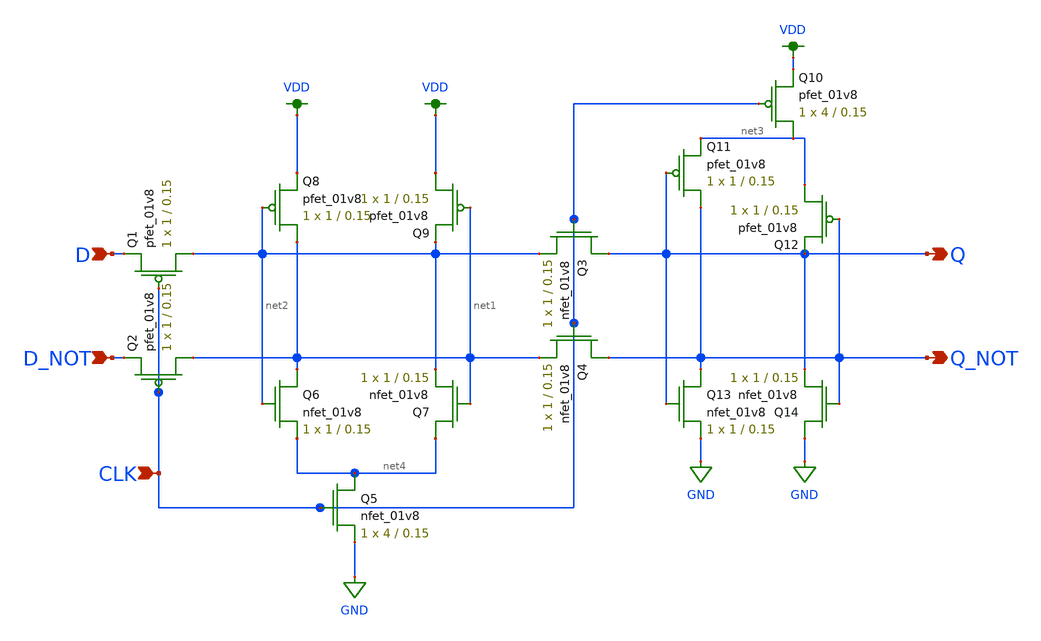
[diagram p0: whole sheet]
** sch_path: miniproject2/CSRL_Latch.sch
**.subckt CSRL_Latch D D_NOT Q Q_NOT CLK
*.ipin D
*.ipin D_NOT
*.opin Q
*.opin Q_NOT
*.ipin CLK
XQ8 net1 net2 VDD VDD sky130_fd_pr__pfet_01v8 L=0.15 W=1 nf=1 ad='int((nf+1)/2) * W/nf * 0.29' as='int((nf+2)/2) * W/nf * 0.29'
+ pd='2*int((nf+1)/2) * (W/nf + 0.29)' ps='2*int((nf+2)/2) * (W/nf + 0.29)' nrd='0.29 / W' nrs='0.29 / W'
+ sa=0 sb=0 sd=0 mult=1 m=1
XQ9 VDD net1 net2 VDD sky130_fd_pr__pfet_01v8 L=0.15 W=1 nf=1 ad='int((nf+1)/2) * W/nf * 0.29' as='int((nf+2)/2) * W/nf * 0.29'
+ pd='2*int((nf+1)/2) * (W/nf + 0.29)' ps='2*int((nf+2)/2) * (W/nf + 0.29)' nrd='0.29 / W' nrs='0.29 / W'
+ sa=0 sb=0 sd=0 mult=1 m=1
XQ1 net2 CLK D VDD sky130_fd_pr__pfet_01v8 L=0.15 W=1 nf=1 ad='int((nf+1)/2) * W/nf * 0.29' as='int((nf+2)/2) * W/nf * 0.29'
+ pd='2*int((nf+1)/2) * (W/nf + 0.29)' ps='2*int((nf+2)/2) * (W/nf + 0.29)' nrd='0.29 / W' nrs='0.29 / W'
+ sa=0 sb=0 sd=0 mult=1 m=1
XQ2 net1 CLK D_NOT VDD sky130_fd_pr__pfet_01v8 L=0.15 W=1 nf=1 ad='int((nf+1)/2) * W/nf * 0.29' as='int((nf+2)/2) * W/nf * 0.29'
+ pd='2*int((nf+1)/2) * (W/nf + 0.29)' ps='2*int((nf+2)/2) * (W/nf + 0.29)' nrd='0.29 / W' nrs='0.29 / W'
+ sa=0 sb=0 sd=0 mult=1 m=1
XQ5 net4 CLK GND GND sky130_fd_pr__nfet_01v8 L=0.15 W=4 nf=1 ad='int((nf+1)/2) * W/nf * 0.29' as='int((nf+2)/2) * W/nf * 0.29'
+ pd='2*int((nf+1)/2) * (W/nf + 0.29)' ps='2*int((nf+2)/2) * (W/nf + 0.29)' nrd='0.29 / W' nrs='0.29 / W'
+ sa=0 sb=0 sd=0 mult=1 m=1
XQ4 Q_NOT CLK net1 GND sky130_fd_pr__nfet_01v8 L=0.15 W=1 nf=1 ad='int((nf+1)/2) * W/nf * 0.29' as='int((nf+2)/2) * W/nf * 0.29'
+ pd='2*int((nf+1)/2) * (W/nf + 0.29)' ps='2*int((nf+2)/2) * (W/nf + 0.29)' nrd='0.29 / W' nrs='0.29 / W'
+ sa=0 sb=0 sd=0 mult=1 m=1
XQ3 Q CLK net2 GND sky130_fd_pr__nfet_01v8 L=0.15 W=1 nf=1 ad='int((nf+1)/2) * W/nf * 0.29' as='int((nf+2)/2) * W/nf * 0.29'
+ pd='2*int((nf+1)/2) * (W/nf + 0.29)' ps='2*int((nf+2)/2) * (W/nf + 0.29)' nrd='0.29 / W' nrs='0.29 / W'
+ sa=0 sb=0 sd=0 mult=1 m=1
XQ6 net1 net2 net4 GND sky130_fd_pr__nfet_01v8 L=0.15 W=1 nf=1 ad='int((nf+1)/2) * W/nf * 0.29' as='int((nf+2)/2) * W/nf * 0.29'
+ pd='2*int((nf+1)/2) * (W/nf + 0.29)' ps='2*int((nf+2)/2) * (W/nf + 0.29)' nrd='0.29 / W' nrs='0.29 / W'
+ sa=0 sb=0 sd=0 mult=1 m=1
XQ7 net4 net1 net2 GND sky130_fd_pr__nfet_01v8 L=0.15 W=1 nf=1 ad='int((nf+1)/2) * W/nf * 0.29' as='int((nf+2)/2) * W/nf * 0.29'
+ pd='2*int((nf+1)/2) * (W/nf + 0.29)' ps='2*int((nf+2)/2) * (W/nf + 0.29)' nrd='0.29 / W' nrs='0.29 / W'
+ sa=0 sb=0 sd=0 mult=1 m=1
XQ13 Q_NOT Q GND GND sky130_fd_pr__nfet_01v8 L=0.15 W=1 nf=1 ad='int((nf+1)/2) * W/nf * 0.29' as='int((nf+2)/2) * W/nf * 0.29'
+ pd='2*int((nf+1)/2) * (W/nf + 0.29)' ps='2*int((nf+2)/2) * (W/nf + 0.29)' nrd='0.29 / W' nrs='0.29 / W'
+ sa=0 sb=0 sd=0 mult=1 m=1
XQ14 GND Q_NOT Q GND sky130_fd_pr__nfet_01v8 L=0.15 W=1 nf=1 ad='int((nf+1)/2) * W/nf * 0.29' as='int((nf+2)/2) * W/nf * 0.29'
+ pd='2*int((nf+1)/2) * (W/nf + 0.29)' ps='2*int((nf+2)/2) * (W/nf + 0.29)' nrd='0.29 / W' nrs='0.29 / W'
+ sa=0 sb=0 sd=0 mult=1 m=1
XQ11 Q_NOT Q net3 VDD sky130_fd_pr__pfet_01v8 L=0.15 W=1 nf=1 ad='int((nf+1)/2) * W/nf * 0.29' as='int((nf+2)/2) * W/nf * 0.29'
+ pd='2*int((nf+1)/2) * (W/nf + 0.29)' ps='2*int((nf+2)/2) * (W/nf + 0.29)' nrd='0.29 / W' nrs='0.29 / W'
+ sa=0 sb=0 sd=0 mult=1 m=1
XQ12 net3 Q_NOT Q VDD sky130_fd_pr__pfet_01v8 L=0.15 W=1 nf=1 ad='int((nf+1)/2) * W/nf * 0.29' as='int((nf+2)/2) * W/nf * 0.29'
+ pd='2*int((nf+1)/2) * (W/nf + 0.29)' ps='2*int((nf+2)/2) * (W/nf + 0.29)' nrd='0.29 / W' nrs='0.29 / W'
+ sa=0 sb=0 sd=0 mult=1 m=1
XQ10 net3 CLK VDD VDD sky130_fd_pr__pfet_01v8 L=0.15 W=4 nf=1 ad='int((nf+1)/2) * W/nf * 0.29' as='int((nf+2)/2) * W/nf * 0.29'
+ pd='2*int((nf+1)/2) * (W/nf + 0.29)' ps='2*int((nf+2)/2) * (W/nf + 0.29)' nrd='0.29 / W' nrs='0.29 / W'
+ sa=0 sb=0 sd=0 mult=1 m=1
**.ends
.GLOBAL GND
.GLOBAL VDD
.end
